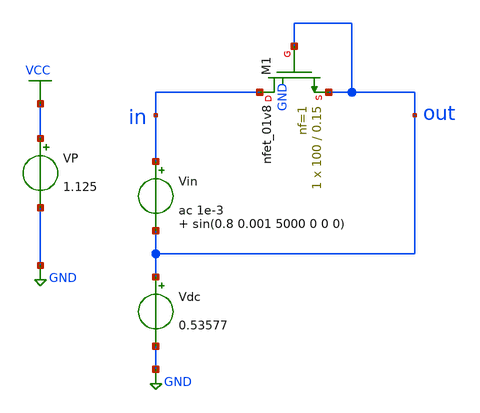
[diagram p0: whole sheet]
** sch_path: Amplifier_Inv/xschem/untitled.sch
**.subckt untitled
VP VCC GND 1.125
Vin in out ac 1e-3 sin(0.8 0.001 5000 0 0 0)
Vdc out GND 0.53577
XM1 in out out GND sky130_fd_pr__nfet_01v8 L=0.15 W=100 nf=1 ad='int((nf+1)/2) * W/nf * 0.29' as='int((nf+2)/2) * W/nf * 0.29'
+ pd='2*int((nf+1)/2) * (W/nf + 0.29)' ps='2*int((nf+2)/2) * (W/nf + 0.29)' nrd='0.29 / W' nrs='0.29 / W'
+ sa=0 sb=0 sd=0 mult=1 m=1
**** begin user architecture code

** opencircuitdesign pdks install
.lib $::SKYWATER_MODELS/sky130.lib.spice tt



.control

  ac lin 100 1 100k
  save all
  let r = (v(out)-v(in))/i(Vin)
  write tb_inv_sky130_a_res_AC_v2.raw r

  tran 0.1u 4m
  save all
  write test.raw

  exit 0
.endc


**** end user architecture code
**.ends
.GLOBAL GND
.GLOBAL VCC
.end
